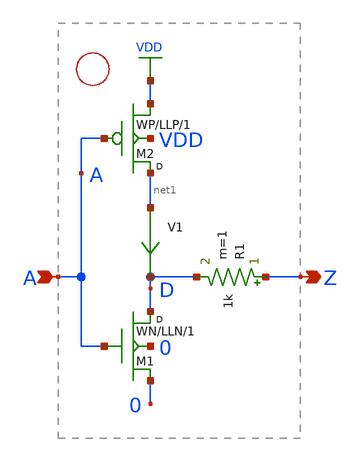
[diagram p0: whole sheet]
** sch_path: xschem_library/examples/cmos_inv.sch
* Copyright (C) 1998-2023 Stefan Frederik Schippers
* This program is free software; you can redistribute it and/or modify
* it under the terms of the GNU General Public License as published by
* the Free Software Foundation; either version 2 of the License, or
* (at your option) any later version.
* This program is distributed in the hope that it will be useful,
* but WITHOUT ANY WARRANTY; without even the implied warranty of
* MERCHANTABILITY or FITNESS FOR A PARTICULAR PURPOSE.  See the
* GNU General Public License for more details.
* You should have received a copy of the GNU General Public License
* along with this program; if not, write to the Free Software
**.subckt cmos_inv Z A
*.opin Z
*.ipin A
M2 net1 A VDD VDD p w=WP l=LLP m=1
M1 D A 0 0 n w=WN l=LLN m=1
R1 Z D 1k m=1
V1 net1 D 0
.save i(v1)
**.ends
.GLOBAL VDD
.end
